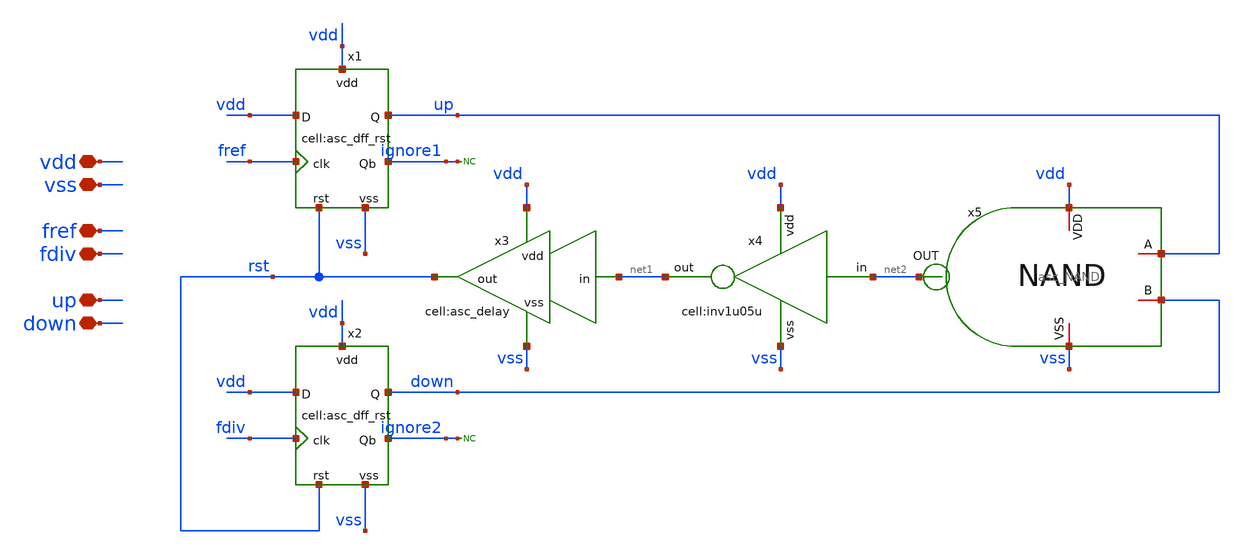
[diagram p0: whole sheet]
** sch_path: designs/libs/core_analog/asc_PFD_DFF/asc_PFD_DFF.sch
**.subckt asc_PFD_DFF vdd vss fref fdiv up down
*.iopin vdd
*.iopin vss
*.iopin fref
*.iopin fdiv
*.iopin up
*.iopin down
x1 fref vdd ignore1 vdd vss up rst asc_dff_rst
x2 fdiv vdd ignore2 vdd vss down rst asc_dff_rst
x4 net2 vdd net1 vss inv1u05u
x3 net1 vss rst vdd asc_delay
x5 vdd net2 up down vss asc_NAND
* noconn ignore1
* noconn ignore2
**.ends
.end
